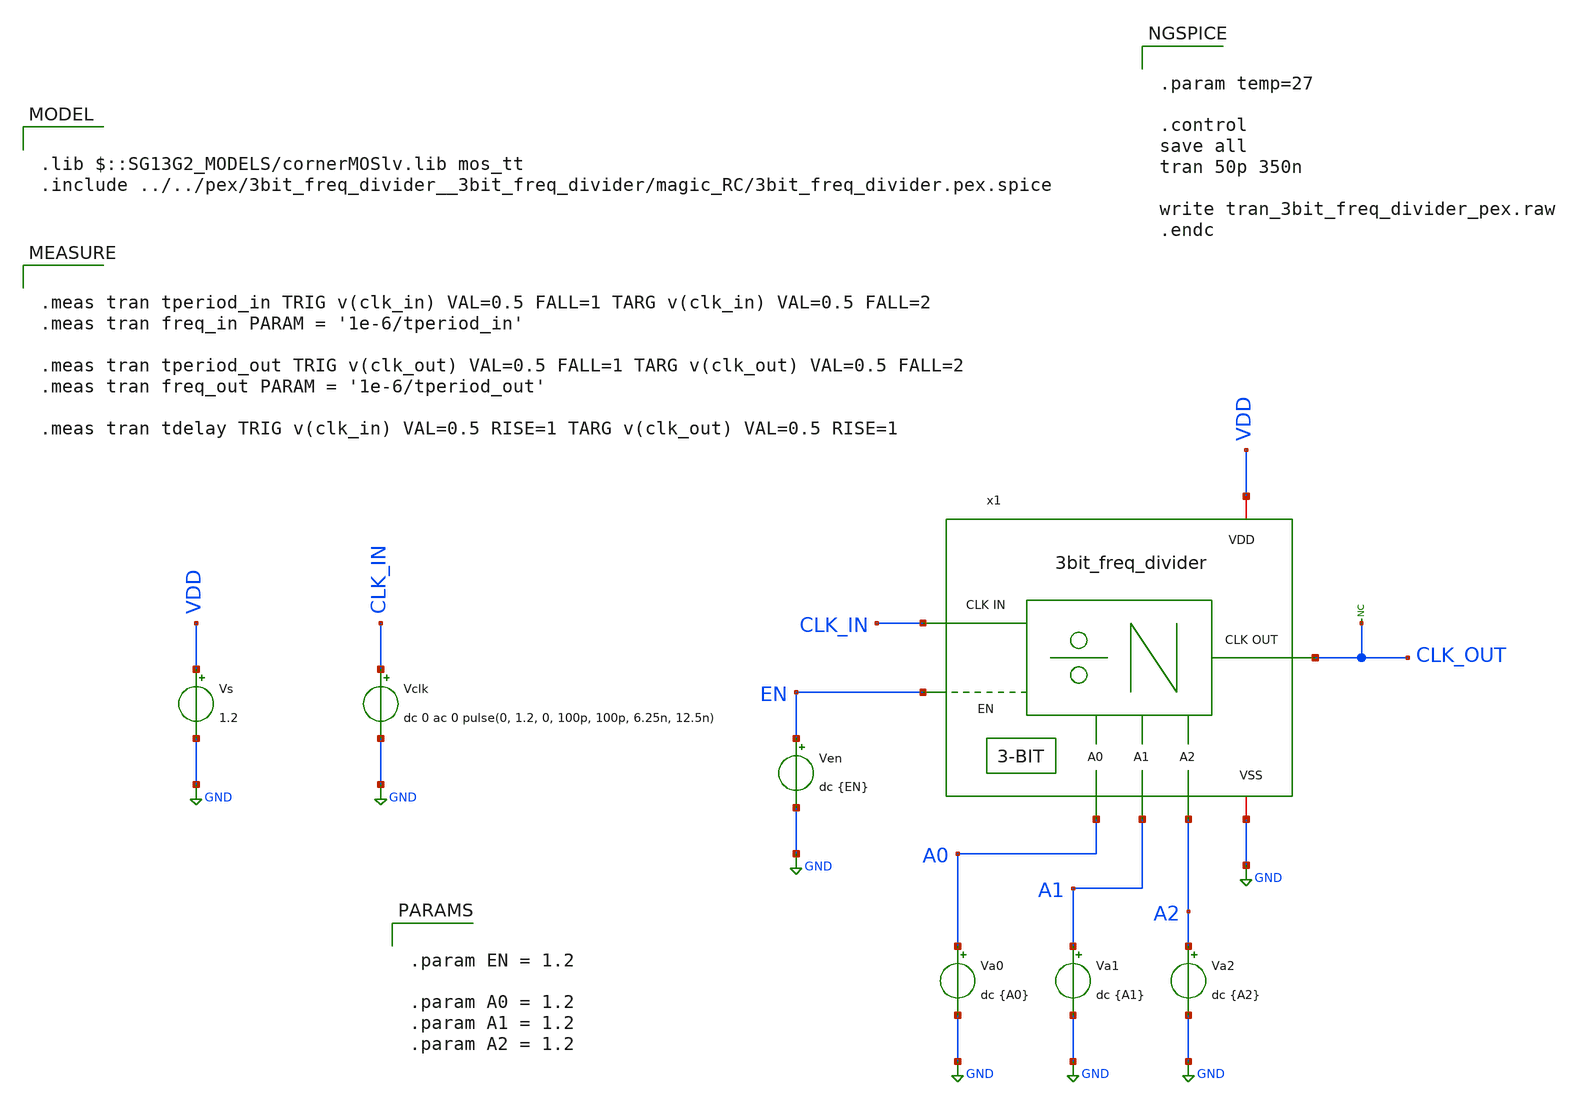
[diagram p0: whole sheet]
** sch_path: Combined_Design/design_data/xschem/3bit_freq_divider_pex_tb.sch

.lib $::SG13G2_MODELS/cornerMOSlv.lib mos_tt
.include ../../pex/3bit_freq_divider__3bit_freq_divider/magic_RC/3bit_freq_divider.pex.spice

**.subckt 3bit_freq_divider_pex_tb
Vs VDD GND 1.2
Vclk CLK_IN GND dc 0 ac 0 pulse(0, 1.2, 0, 100p, 100p, 6.25n, 12.5n)
* noconn CLK_OUT
Ven EN GND dc {EN}
Va1 A1 GND dc {A1}
Va2 A2 GND dc {A2}
x1 A0 CLK_IN EN CLK_OUT A1 VDD GND A2 3bit_freq_divider
Va0 A0 GND dc {A0}
**** begin user architecture code


.meas tran tperiod_in TRIG v(clk_in) VAL=0.5 FALL=1 TARG v(clk_in) VAL=0.5 FALL=2
.meas tran freq_in PARAM = '1e-6/tperiod_in'

.meas tran tperiod_out TRIG v(clk_out) VAL=0.5 FALL=1 TARG v(clk_out) VAL=0.5 FALL=2
.meas tran freq_out PARAM = '1e-6/tperiod_out'

.meas tran tdelay TRIG v(clk_in) VAL=0.5 RISE=1 TARG v(clk_out) VAL=0.5 RISE=1




.param EN = 1.2

.param A0 = 1.2
.param A1 = 1.2
.param A2 = 1.2




.param temp=27

.control
save all
tran 50p 350n

write tran_3bit_freq_divider_pex.raw
.endc




RLEAK_C418  x1.a_n232_n2530#  VSS  1e11
RLEAK_C419  x1.a_n232_n2508#  VSS  1e11
RLEAK_C443  x1.a_n232_n774#   VSS  1e11
RLEAK_C444  x1.a_n232_n752#   VSS  1e11


**** end user architecture code
**.ends
.GLOBAL GND
.end
